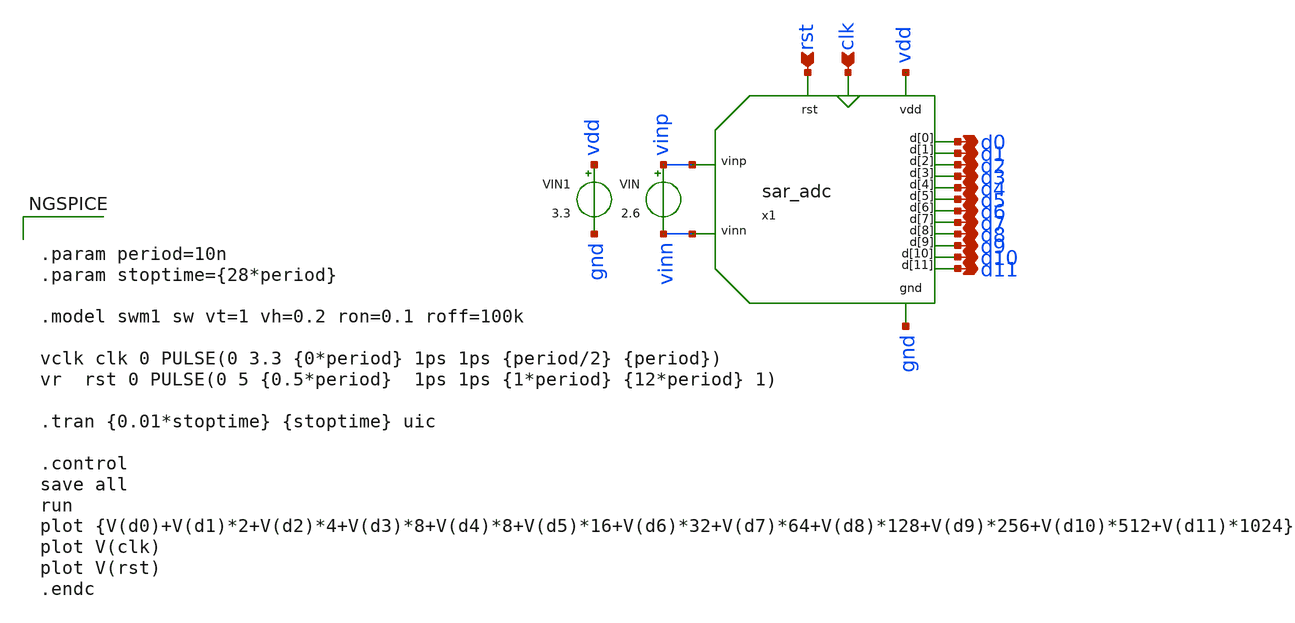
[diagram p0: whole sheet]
** sch_path: SAR_ADC/xschem/test/tb_sar_adc.sch
**.subckt tb_sar_adc rst clk d0 d1 d2 d3 d4 d5 d6 d7 d8 d9 d10 d11
*.ipin rst
*.ipin clk
*.opin d0
*.opin d1
*.opin d2
*.opin d3
*.opin d4
*.opin d5
*.opin d6
*.opin d7
*.opin d8
*.opin d9
*.opin d10
*.opin d11
x1 vinp d0 rst clk vinn gnd vdd d1 d2 d3 d4 d5 d6 d7 d8 d9 d10 d11 sar_adc
VIN vinp vinn 2.6
VIN1 vdd gnd 3.3
**** begin user architecture code


.param period=10n
.param stoptime={28*period}

.model swm1 sw vt=1 vh=0.2 ron=0.1 roff=100k

vclk clk 0 PULSE(0 3.3 {0*period} 1ps 1ps {period/2} {period})
vr  rst 0 PULSE(0 5 {0.5*period}  1ps 1ps {1*period} {12*period} 1)

.tran {0.01*stoptime} {stoptime} uic

.control
save all
run
plot {V(d0)+V(d1)*2+V(d2)*4+V(d3)*8+V(d4)*8+V(d5)*16+V(d6)*32+V(d7)*64+V(d8)*128+V(d9)*256+V(d10)*512+V(d11)*1024}
plot V(clk)
plot V(rst)
.endc



.include $::PDK_ROOT/gf180mcuD/libs.tech/ngspice/design.ngspice
.include [pwd]/../spice/sar_logic.spice
.lib $::PDK_ROOT/gf180mcuD/libs.tech/ngspice/sm141064.ngspice mimcap_statistical
.lib $::PDK_ROOT/gf180mcuD/libs.tech/ngspice/sm141064.ngspice cap_mim
.lib $::PDK_ROOT/gf180mcuD/libs.tech/ngspice/sm141064.ngspice typical

**** end user architecture code
**.ends

* expanding   symbol:  ../spice/sar_adc.sym # of pins=18
** sym_path: SAR_ADC/xschem/spice/sar_adc.sym
** sch_path: SAR_ADC/xschem/spice/sar_adc.sch
.subckt sar_adc vinp d[0] rst clk vinn gnd vdd d[1] d[2] d[3] d[4] d[5] d[6] d[7] d[8] d[9] d[10]
+ d[11]
*.ipin vinn
*.ipin vinp
*.ipin clk
*.ipin rst
*.ipin vdd
*.ipin gnd
*.opin d[0]
*.opin d[1]
*.opin d[2]
*.opin d[3]
*.opin d[4]
*.opin d[5]
*.opin d[6]
*.opin d[7]
*.opin d[8]
*.opin d[9]
*.opin d[10]
*.opin d[11]
x1 net5 net1 d[9] d[7] d[0] d[11] d[3] d[4] d[2] d[1] d[8] d[6] d[5] d[10] gnd vdd cdac cu=5u
x2 net4 net2 d[9] d[7] d[0] d[11] d[3] d[4] d[2] d[1] d[8] d[6] d[5] d[10] gnd vdd cdac cu=5u
X5 vdd gnd net4 net5 net3 clk Preamp-Strong-Latch
X6 d[11] net3 rst clk net6 vdd gnd d[10] d[9] d[8] d[7] d[6] d[5] d[4] d[3] d[2] d[1] d[0] sar_logic
S1 vinp net2 net6 gnd swm1
S2 vinn net1 net6 gnd swm1
.ends


* expanding   symbol:  ../spice/cdac.sym # of pins=16
** sym_path: SAR_ADC/xschem/spice/cdac.sym
** sch_path: SAR_ADC/xschem/spice/cdac.sch
.subckt cdac out in d[9] d[7] d[0] d[11] d[3] d[4] d[2] d[1] d[8] d[6] d[5] d[10] gnd vdd  cu=5u
*.ipin d[0]
*.ipin d[1]
*.ipin d[2]
*.ipin d[3]
*.ipin d[4]
*.ipin d[5]
*.ipin d[6]
*.ipin d[7]
*.ipin d[8]
*.ipin d[9]
*.ipin d[10]
*.ipin d[11]
*.ipin vdd
*.ipin gnd
*.opin out
*.iopin in
x1 in vdd gnd d[0] cdac_line CW={sqrt(2)*cu} CL={sqrt(2)*cu}
x2 in vdd gnd d[1] cdac_line CW={sqrt(3)*cu} CL={sqrt(3)*cu}
x3 in vdd gnd d[2] cdac_line CW={sqrt(4)*cu} CL={sqrt(4)*cu}
x4 in vdd gnd d[3] cdac_line CW={sqrt(8)*cu} CL={sqrt(8)*cu}
x5 in vdd gnd d[4] cdac_line CW={sqrt(16)*cu} CL={sqrt(16)*cu}
x6 in vdd gnd d[5] cdac_line CW={sqrt(32)*cu} CL={sqrt(32)*cu}
XCA out in cap_mim_1f5fF c_width={cu} c_length={cu} m=1
x7 out vdd gnd d[6] cdac_line CW={sqrt(1)*cu} CL={sqrt(1)*cu}
x8 out vdd gnd d[7] cdac_line CW={sqrt(2)*cu} CL={sqrt(2)*cu}
x9 out vdd gnd d[8] cdac_line CW={sqrt(4)*cu} CL={sqrt(4)*cu}
x10 out vdd gnd d[9] cdac_line CW={sqrt(8)*cu} CL={sqrt(8)*cu}
x11 out vdd gnd d[10] cdac_line CW={sqrt(16)*cu} CL={sqrt(16)*cu}
x12 out vdd gnd d[11] cdac_line CW={sqrt(32)*cu} CL={sqrt(32)*cu}
R1 out in 100T m=1
XC0 in gnd cap_mim_1f5fF c_width={cu} c_length={cu} m=1
.ends


* expanding   symbol:  ../spice/Preamp-Strong-Latch.sym # of pins=6
** sym_path: SAR_ADC/xschem/spice/symbols/Preamp-Strong-Latch.sym
** sch_path: SAR_ADC/xschem/spice/symbols/Preamp-Strong-Latch.sch
.subckt Preamp-Strong-Latch V GND Vinp Vinn OUT clk
*.iopin V
*.iopin GND
*.iopin Vinp
*.iopin Vinn
*.iopin clk
*.iopin OUT
X1 net4 V GND net5 OUT net7 SR_nor
x2 V GND net4 net8 inv cl=0.28u wp=0.44u wn=0.22u
x3 V GND net8 net3 inv cl=0.28u wp=0.44u wn=0.22u
x4 V GND net5 net9 inv cl=0.28u wp=0.44u wn=0.22u
x5 V GND net9 net6 inv cl=0.28u wp=0.44u wn=0.22u
X6 V GND net2 net1 clk net3 net6 strongarm
X7 V GND Vinp clk net1 net2 Vinn preamp
.ends


* expanding   symbol:  ../spice/sar_logic.sym # of pins=18
** sym_path: SAR_ADC/xschem/spice/sar_logic.sym
** sch_path: SAR_ADC/xschem/spice/sar_logic.sch
.subckt sar_logic q11 data_in reset clock eoc vdd gnd q10 q9 q8 q7 q6 q5 q4 q3 q2 q1 q0
*.opin q11
*.opin eoc
*.ipin clock
*.ipin data_in
*.ipin reset
*.ipin gnd
*.ipin vdd
*.opin q10
*.opin q9
*.opin q8
*.opin q7
*.opin q6
*.opin q5
*.opin q4
*.opin q3
*.opin q2
*.opin q1
*.opin q0
XFF0 eoc clock reset gnd net14 gnd vdd ff
XFF1 net14 clock vdd reset net1 gnd vdd ff
XFF2 net1 clock vdd reset net2 gnd vdd ff
XFF14 data_in q10 net1 reset q11 gnd vdd ff
XFF3 net2 clock vdd reset net3 gnd vdd ff
XFF15 data_in q9 net2 reset q10 gnd vdd ff
XFF4 net3 clock vdd reset net4 gnd vdd ff
XFF16 data_in q8 net3 reset q9 gnd vdd ff
XFF17 data_in q7 net4 reset q8 gnd vdd ff
XFF5 net4 clock vdd reset net5 gnd vdd ff
XFF18 data_in q6 net5 reset q7 gnd vdd ff
XFF19 data_in q5 net6 reset q6 gnd vdd ff
XFF6 net5 clock vdd reset net6 gnd vdd ff
XFF7 net6 clock vdd reset net7 gnd vdd ff
XFF8 net7 clock vdd reset net8 gnd vdd ff
XFF9 net8 clock vdd reset net9 gnd vdd ff
XFF20 data_in q4 net7 reset q5 gnd vdd ff
XFF21 data_in q3 net8 reset q4 gnd vdd ff
XFF22 data_in q2 net9 reset q3 gnd vdd ff
XFF23 data_in q1 net10 reset q2 gnd vdd ff
XFF10 net9 clock vdd reset net10 gnd vdd ff
XFF11 net10 clock vdd reset net11 gnd vdd ff
XFF12 net11 clock vdd reset net12 gnd vdd ff
XFF24 data_in q0 net11 reset q1 gnd vdd ff
XFF13 net12 clock vdd reset eoc gnd vdd ff
XFF25 data_in net13 net12 reset q0 gnd vdd ff
XFF26 gnd gnd eoc reset net13 gnd vdd ff
.ends


* expanding   symbol:  /foss/designs/sar_adc/xschem/spice/cdac_line.sym # of pins=4
** sym_path: SAR_ADC/xschem/spice/cdac_line.sym
** sch_path: SAR_ADC/xschem/spice/cdac_line.sch
.subckt cdac_line vout vdd gnd vin  CW=1e-6 CL=1e-6
*.ipin vdd
*.ipin gnd
*.ipin vin
*.opin vout
x1 vdd gnd net1 net2 inv cl=0.28u wp=0.66u wn=0.22u
XC1 vout net1 cap_mim_2f0fF c_width=CW c_length=CL m=1
x2 vdd gnd net2 vin inv cl=0.28u wp=0.66u wn=0.22u
.ends


* expanding   symbol:  symbols/SR_nor.sym # of pins=6
** sym_path: SAR_ADC/xschem/designs/SR_nor.sym
** sch_path: SAR_ADC/xschem/designs/SR_nor.sch
.subckt SR_nor S V GND R Q Qn
*.iopin V
*.iopin GND
*.iopin S
*.iopin R
*.iopin Qn
*.iopin Q
X1 S Q Qn GND V norgate
X2 Qn R Q GND V norgate
.ends


* expanding   symbol:  symbols/inv.sym # of pins=4
** sym_path: SAR_ADC/xschem/spice/inv.sym
** sch_path: SAR_ADC/xschem/spice/inv.sch
.subckt inv vdd gnd vout vin  cl=0.28u wp=0.44u wn=0.22u
*.ipin gnd
*.ipin vdd
*.ipin vin
*.opin vout
XM1 gnd vin vout gnd nfet_03v3 L=0.28u W=4u nf=1 ad='int((nf+1)/2) * W/nf * 0.18u' as='int((nf+2)/2) * W/nf * 0.18u'
+ pd='2*int((nf+1)/2) * (W/nf + 0.18u)' ps='2*int((nf+2)/2) * (W/nf + 0.18u)' nrd='0.18u / W' nrs='0.18u / W'
+ sa=0 sb=0 sd=0 m=1
XM2 vdd vin vout vdd pfet_03v3 L=0.28u W=4u nf=1 ad='int((nf+1)/2) * W/nf * 0.18u' as='int((nf+2)/2) * W/nf * 0.18u'
+ pd='2*int((nf+1)/2) * (W/nf + 0.18u)' ps='2*int((nf+2)/2) * (W/nf + 0.18u)' nrd='0.18u / W' nrs='0.18u / W'
+ sa=0 sb=0 sd=0 m=1
.ends


* expanding   symbol:  symbols/strongarm.sym # of pins=7
** sym_path: SAR_ADC/xschem/designs/strongarm.sym
** sch_path: SAR_ADC/xschem/designs/strongarm.sch
.subckt strongarm V GND Vin1 Vin2 CLK Vout1 Vout2
*.iopin V
*.iopin Vout1
*.iopin Vin1
*.iopin Vin2
*.iopin Vout2
*.iopin CLK
*.iopin GND
XM1 net3 Vout2 V V pfet_03v3 L=0.28u W=2u nf=1 ad='int((nf+1)/2) * W/nf * 0.18u' as='int((nf+2)/2) * W/nf * 0.18u'
+ pd='2*int((nf+1)/2) * (W/nf + 0.18u)' ps='2*int((nf+2)/2) * (W/nf + 0.18u)' nrd='0.18u / W' nrs='0.18u / W'
+ sa=0 sb=0 sd=0 m=1
XM2 Vout1 net1 GND GND nfet_03v3 L=0.28u W=2u nf=1 ad='int((nf+1)/2) * W/nf * 0.18u' as='int((nf+2)/2) * W/nf * 0.18u'
+ pd='2*int((nf+1)/2) * (W/nf + 0.18u)' ps='2*int((nf+2)/2) * (W/nf + 0.18u)' nrd='0.18u / W' nrs='0.18u / W'
+ sa=0 sb=0 sd=0 m=1
XM3 Vout2 Vout1 GND GND nfet_03v3 L=0.28u W=2u nf=1 ad='int((nf+1)/2) * W/nf * 0.18u' as='int((nf+2)/2) * W/nf * 0.18u'
+ pd='2*int((nf+1)/2) * (W/nf + 0.18u)' ps='2*int((nf+2)/2) * (W/nf + 0.18u)' nrd='0.18u / W' nrs='0.18u / W'
+ sa=0 sb=0 sd=0 m=1
XM4 Vout2 net1 GND GND nfet_03v3 L=0.28u W=2u nf=1 ad='int((nf+1)/2) * W/nf * 0.18u' as='int((nf+2)/2) * W/nf * 0.18u'
+ pd='2*int((nf+1)/2) * (W/nf + 0.18u)' ps='2*int((nf+2)/2) * (W/nf + 0.18u)' nrd='0.18u / W' nrs='0.18u / W'
+ sa=0 sb=0 sd=0 m=1
XM5 Vout1 Vout2 GND GND nfet_03v3 L=0.28u W=2u nf=1 ad='int((nf+1)/2) * W/nf * 0.18u' as='int((nf+2)/2) * W/nf * 0.18u'
+ pd='2*int((nf+1)/2) * (W/nf + 0.18u)' ps='2*int((nf+2)/2) * (W/nf + 0.18u)' nrd='0.18u / W' nrs='0.18u / W'
+ sa=0 sb=0 sd=0 m=1
XM6 net2 Vout1 V V pfet_03v3 L=0.28u W=2u nf=1 ad='int((nf+1)/2) * W/nf * 0.18u' as='int((nf+2)/2) * W/nf * 0.18u'
+ pd='2*int((nf+1)/2) * (W/nf + 0.18u)' ps='2*int((nf+2)/2) * (W/nf + 0.18u)' nrd='0.18u / W' nrs='0.18u / W'
+ sa=0 sb=0 sd=0 m=1
XM7 Vout1 Vin1 net3 V pfet_03v3 L=0.28u W=10u nf=1 ad='int((nf+1)/2) * W/nf * 0.18u' as='int((nf+2)/2) * W/nf * 0.18u'
+ pd='2*int((nf+1)/2) * (W/nf + 0.18u)' ps='2*int((nf+2)/2) * (W/nf + 0.18u)' nrd='0.18u / W' nrs='0.18u / W'
+ sa=0 sb=0 sd=0 m=1
XM8 Vout2 Vin2 net2 V pfet_03v3 L=0.28u W=10u nf=1 ad='int((nf+1)/2) * W/nf * 0.18u' as='int((nf+2)/2) * W/nf * 0.18u'
+ pd='2*int((nf+1)/2) * (W/nf + 0.18u)' ps='2*int((nf+2)/2) * (W/nf + 0.18u)' nrd='0.18u / W' nrs='0.18u / W'
+ sa=0 sb=0 sd=0 m=1
x1 V GND net4 CLK inv cl=0.28u wp=0.44u wn=0.22u wx=4u
x2 V GND net1 net4 inv cl=0.28u wp=0.44u wn=0.22u wx=4u
.ends


* expanding   symbol:  symbols/preamp.sym # of pins=7
** sym_path: SAR_ADC/xschem/designs/preamp.sym
** sch_path: SAR_ADC/xschem/designs/preamp.sch
.subckt preamp V GND Vin1 clk Vout1 Vout2 Vin2
*.iopin V
*.iopin GND
*.iopin Vout2
*.iopin Vout1
*.iopin clk
*.iopin Vin2
*.iopin Vin1
XM26 Vout2 clk GND GND nfet_03v3 L=.5u W=.22u nf=1 ad='int((nf+1)/2) * W/nf * 0.18u' as='int((nf+2)/2) * W/nf * 0.18u'
+ pd='2*int((nf+1)/2) * (W/nf + 0.18u)' ps='2*int((nf+2)/2) * (W/nf + 0.18u)' nrd='0.18u / W' nrs='0.18u / W'
+ sa=0 sb=0 sd=0 m=1
XM27 Vout1 clk GND GND nfet_03v3 L=.5u W=.22u nf=1 ad='int((nf+1)/2) * W/nf * 0.18u' as='int((nf+2)/2) * W/nf * 0.18u'
+ pd='2*int((nf+1)/2) * (W/nf + 0.18u)' ps='2*int((nf+2)/2) * (W/nf + 0.18u)' nrd='0.18u / W' nrs='0.18u / W'
+ sa=0 sb=0 sd=0 m=1
XM24 Vout1 Vin2 net1 V pfet_03v3 L=.28u W=8u nf=1 ad='int((nf+1)/2) * W/nf * 0.18u' as='int((nf+2)/2) * W/nf * 0.18u'
+ pd='2*int((nf+1)/2) * (W/nf + 0.18u)' ps='2*int((nf+2)/2) * (W/nf + 0.18u)' nrd='0.18u / W' nrs='0.18u / W'
+ sa=0 sb=0 sd=0 m=1
XM25 Vout2 Vin1 net1 V pfet_03v3 L=.28u W=8u nf=1 ad='int((nf+1)/2) * W/nf * 0.18u' as='int((nf+2)/2) * W/nf * 0.18u'
+ pd='2*int((nf+1)/2) * (W/nf + 0.18u)' ps='2*int((nf+2)/2) * (W/nf + 0.18u)' nrd='0.18u / W' nrs='0.18u / W'
+ sa=0 sb=0 sd=0 m=1
XM1 V clk net1 V pfet_03v3 L=2u W=1u nf=1 ad='int((nf+1)/2) * W/nf * 0.18u' as='int((nf+2)/2) * W/nf * 0.18u'
+ pd='2*int((nf+1)/2) * (W/nf + 0.18u)' ps='2*int((nf+2)/2) * (W/nf + 0.18u)' nrd='0.18u / W' nrs='0.18u / W'
+ sa=0 sb=0 sd=0 m=1
.ends


* expanding   symbol:  /foss/designs/sar_adc/xschem/spice/ff.sym # of pins=7
** sym_path: SAR_ADC/xschem/spice/ff.sym
** sch_path: SAR_ADC/xschem/spice/ff.sch
.subckt ff data_in clock set reset data_out gnd vdd
*.ipin data_in
*.ipin clock
*.ipin vdd
*.ipin gnd
*.opin data_out
*.ipin set
*.ipin reset
XFF1 net2 net3 net4 clock net1 vdd gnd gnd gnd gf180mcu_fd_sc_mcu7t5v0__dffrsnq_1
x1 vdd gnd net2 data_in inv cl=0.28u wp=0.44u wn=0.22u
x2 vdd gnd net4 reset inv cl=0.28u wp=0.44u wn=0.22u
x3 vdd gnd net3 set inv cl=0.28u wp=0.44u wn=0.22u
x4 vdd gnd data_out net1 inv cl=0.28u wp=0.44u wn=0.22u
.ends


* expanding   symbol:  norgate.sym # of pins=5
** sym_path: SAR_ADC/xschem/designs/norgate.sym
** sch_path: SAR_ADC/xschem/designs/norgate.sch
.subckt norgate A B Z GND V
*.iopin GND
*.iopin A
*.iopin B
*.iopin V
*.iopin Z
XM3 V A net2 V pfet_03v3 L=0.28u W=0.22u nf=1 ad='int((nf+1)/2) * W/nf * 0.18u' as='int((nf+2)/2) * W/nf * 0.18u'
+ pd='2*int((nf+1)/2) * (W/nf + 0.18u)' ps='2*int((nf+2)/2) * (W/nf + 0.18u)' nrd='0.18u / W' nrs='0.18u / W'
+ sa=0 sb=0 sd=0 m=1
XM6 net2 B Z V pfet_03v3 L=0.28u W=0.22u nf=1 ad='int((nf+1)/2) * W/nf * 0.18u' as='int((nf+2)/2) * W/nf * 0.18u'
+ pd='2*int((nf+1)/2) * (W/nf + 0.18u)' ps='2*int((nf+2)/2) * (W/nf + 0.18u)' nrd='0.18u / W' nrs='0.18u / W'
+ sa=0 sb=0 sd=0 m=1
XM9 V B net1 V pfet_03v3 L=0.28u W=0.22u nf=1 ad='int((nf+1)/2) * W/nf * 0.18u' as='int((nf+2)/2) * W/nf * 0.18u'
+ pd='2*int((nf+1)/2) * (W/nf + 0.18u)' ps='2*int((nf+2)/2) * (W/nf + 0.18u)' nrd='0.18u / W' nrs='0.18u / W'
+ sa=0 sb=0 sd=0 m=1
XM12 net1 A Z V pfet_03v3 L=0.28u W=0.22u nf=1 ad='int((nf+1)/2) * W/nf * 0.18u' as='int((nf+2)/2) * W/nf * 0.18u'
+ pd='2*int((nf+1)/2) * (W/nf + 0.18u)' ps='2*int((nf+2)/2) * (W/nf + 0.18u)' nrd='0.18u / W' nrs='0.18u / W'
+ sa=0 sb=0 sd=0 m=1
XM2 Z B GND GND nfet_03v3 L=0.28u W=0.22u nf=1 ad='int((nf+1)/2) * W/nf * 0.18u' as='int((nf+2)/2) * W/nf * 0.18u'
+ pd='2*int((nf+1)/2) * (W/nf + 0.18u)' ps='2*int((nf+2)/2) * (W/nf + 0.18u)' nrd='0.18u / W' nrs='0.18u / W'
+ sa=0 sb=0 sd=0 m=1
XM4 Z A GND GND nfet_03v3 L=0.28u W=0.22u nf=1 ad='int((nf+1)/2) * W/nf * 0.18u' as='int((nf+2)/2) * W/nf * 0.18u'
+ pd='2*int((nf+1)/2) * (W/nf + 0.18u)' ps='2*int((nf+2)/2) * (W/nf + 0.18u)' nrd='0.18u / W' nrs='0.18u / W'
+ sa=0 sb=0 sd=0 m=1
.ends

.end
